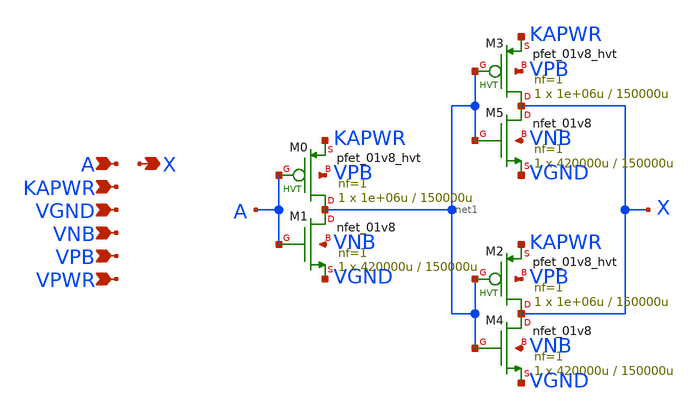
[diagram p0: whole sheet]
** sch_path: schematics/lpflow_clkbufkapwr/sky130_fd_sc_hd__lpflow_clkbufkapwr_2.sch
**.subckt sky130_fd_sc_hd__lpflow_clkbufkapwr_2 A KAPWR VGND VNB VPB VPWR X
*.ipin A
*.ipin KAPWR
*.ipin VGND
*.ipin VNB
*.ipin VPB
*.ipin VPWR
*.opin X
XM0 net1 A KAPWR VPB sky130_fd_pr__pfet_01v8_hvt L=150000u W=1e+06u nf=1 ad='int((1 + 1)/2) * 1e+06u / 1 * 0.29'
+ as='int((1 + 2)/2) * 1e+06u / 1 * 0.29' pd='2*int((1 + 1)/2) * (1e+06u / 1 + 0.29)' ps='2*int((1 + 2)/2) * (1e+06u / 1 + 0.29)'
+ nrd='0.29 / 1e+06u ' nrs='0.29 / 1e+06u ' sa=0 sb=0 sd=0 mult=1 m=1
XM2 X net1 KAPWR VPB sky130_fd_pr__pfet_01v8_hvt L=150000u W=1e+06u nf=1 ad='int((1 + 1)/2) * 1e+06u / 1 * 0.29'
+ as='int((1 + 2)/2) * 1e+06u / 1 * 0.29' pd='2*int((1 + 1)/2) * (1e+06u / 1 + 0.29)' ps='2*int((1 + 2)/2) * (1e+06u / 1 + 0.29)'
+ nrd='0.29 / 1e+06u ' nrs='0.29 / 1e+06u ' sa=0 sb=0 sd=0 mult=1 m=1
XM3 X net1 KAPWR VPB sky130_fd_pr__pfet_01v8_hvt L=150000u W=1e+06u nf=1 ad='int((1 + 1)/2) * 1e+06u / 1 * 0.29'
+ as='int((1 + 2)/2) * 1e+06u / 1 * 0.29' pd='2*int((1 + 1)/2) * (1e+06u / 1 + 0.29)' ps='2*int((1 + 2)/2) * (1e+06u / 1 + 0.29)'
+ nrd='0.29 / 1e+06u ' nrs='0.29 / 1e+06u ' sa=0 sb=0 sd=0 mult=1 m=1
XM1 net1 A VGND VNB sky130_fd_pr__nfet_01v8 L=150000u W=420000u nf=1 ad='int((1 + 1)/2) * 420000u / 1 * 0.29'
+ as='int((1 + 2)/2) * 420000u / 1 * 0.29' pd='2*int((1 + 1)/2) * (420000u / 1 + 0.29)' ps='2*int((1 + 2)/2) * (420000u / 1 + 0.29)'
+ nrd='0.29 / 420000u ' nrs='0.29 / 420000u ' sa=0 sb=0 sd=0 mult=1 m=1
XM4 X net1 VGND VNB sky130_fd_pr__nfet_01v8 L=150000u W=420000u nf=1 ad='int((1 + 1)/2) * 420000u / 1 * 0.29'
+ as='int((1 + 2)/2) * 420000u / 1 * 0.29' pd='2*int((1 + 1)/2) * (420000u / 1 + 0.29)' ps='2*int((1 + 2)/2) * (420000u / 1 + 0.29)'
+ nrd='0.29 / 420000u ' nrs='0.29 / 420000u ' sa=0 sb=0 sd=0 mult=1 m=1
XM5 X net1 VGND VNB sky130_fd_pr__nfet_01v8 L=150000u W=420000u nf=1 ad='int((1 + 1)/2) * 420000u / 1 * 0.29'
+ as='int((1 + 2)/2) * 420000u / 1 * 0.29' pd='2*int((1 + 1)/2) * (420000u / 1 + 0.29)' ps='2*int((1 + 2)/2) * (420000u / 1 + 0.29)'
+ nrd='0.29 / 420000u ' nrs='0.29 / 420000u ' sa=0 sb=0 sd=0 mult=1 m=1
**.ends
.end
